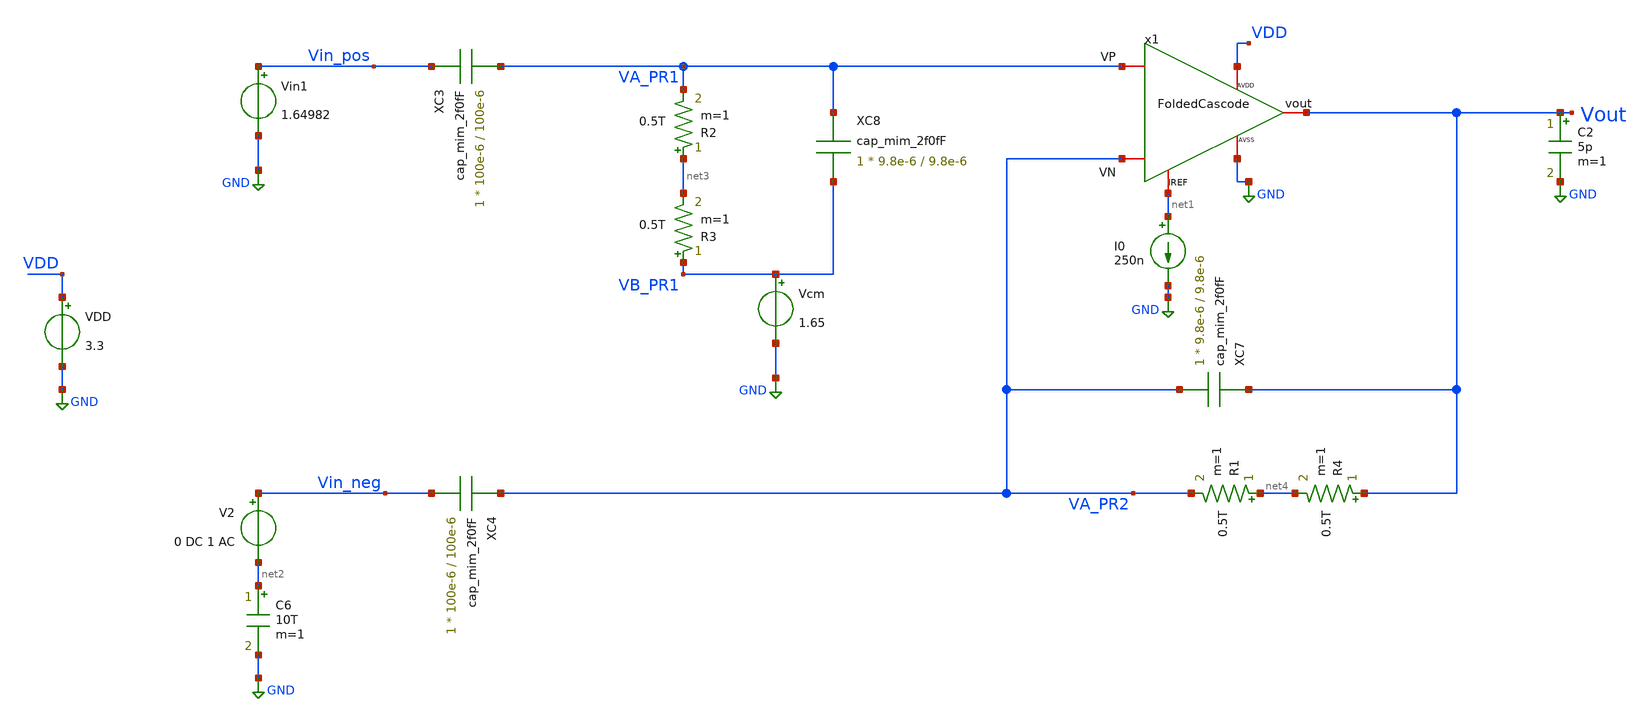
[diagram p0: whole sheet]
** sch_path: TIA_Filter/TB_filter_noPR_ac.sch
**.subckt TB_filter_noPR_ac
VDD VDD GND 3.3
C2 Vout GND 5p m=1
x1 VA_PR1 VA_PR2 Vout net1 VDD GND FoldedCascode
I0 net1 GND 250n
Vcm VB_PR1 GND 1.65
Vin1 Vin_pos GND 1.64982
V2 Vin_neg net2 0 DC 1 AC
C6 net2 GND 10T m=1
R1 net4 VA_PR2 0.5T m=1
R2 net3 VA_PR1 0.5T m=1
R3 VB_PR1 net3 0.5T m=1
R4 Vout net4 0.5T m=1
XC8 VA_PR1 VB_PR1 cap_mim_2f0fF c_width=9.8e-6 c_length=9.8e-6 m=1
XC7 Vout VA_PR2 cap_mim_2f0fF c_width=9.8e-6 c_length=9.8e-6 m=1
XC3 Vin_pos VA_PR1 cap_mim_2f0fF c_width=100e-6 c_length=100e-6 m=1
XC4 VA_PR2 Vin_neg cap_mim_2f0fF c_width=100e-6 c_length=100e-6 m=1
**** begin user architecture code

.include $::180MCU_MODELS/design.ngspice
.lib $::180MCU_MODELS/sm141064.ngspice typical
.lib $::180MCU_MODELS/sm141064.ngspice cap_mim
.lib $::180MCU_MODELS/sm141064.ngspice res_typical
.lib $::180MCU_MODELS/sm141064.ngspice moscap_typical
.lib $::180MCU_MODELS/sm141064.ngspice mimcap_typical



.option gmin=1e-16

.param ibias = 1p
.param it_amp = 2p

.control
save all

*tran 10u 10m
*remzerovec
*write TB_TIA_ac.raw
*set appendwrite

op
remzerovec
write TB_filter_noPR_ac.raw
set appendwrite

ac dec 10 1m 1e8
remzerovec
write TB_filter_noPR_ac.raw


.endc


**** end user architecture code
**.ends
.GLOBAL GND
.end
